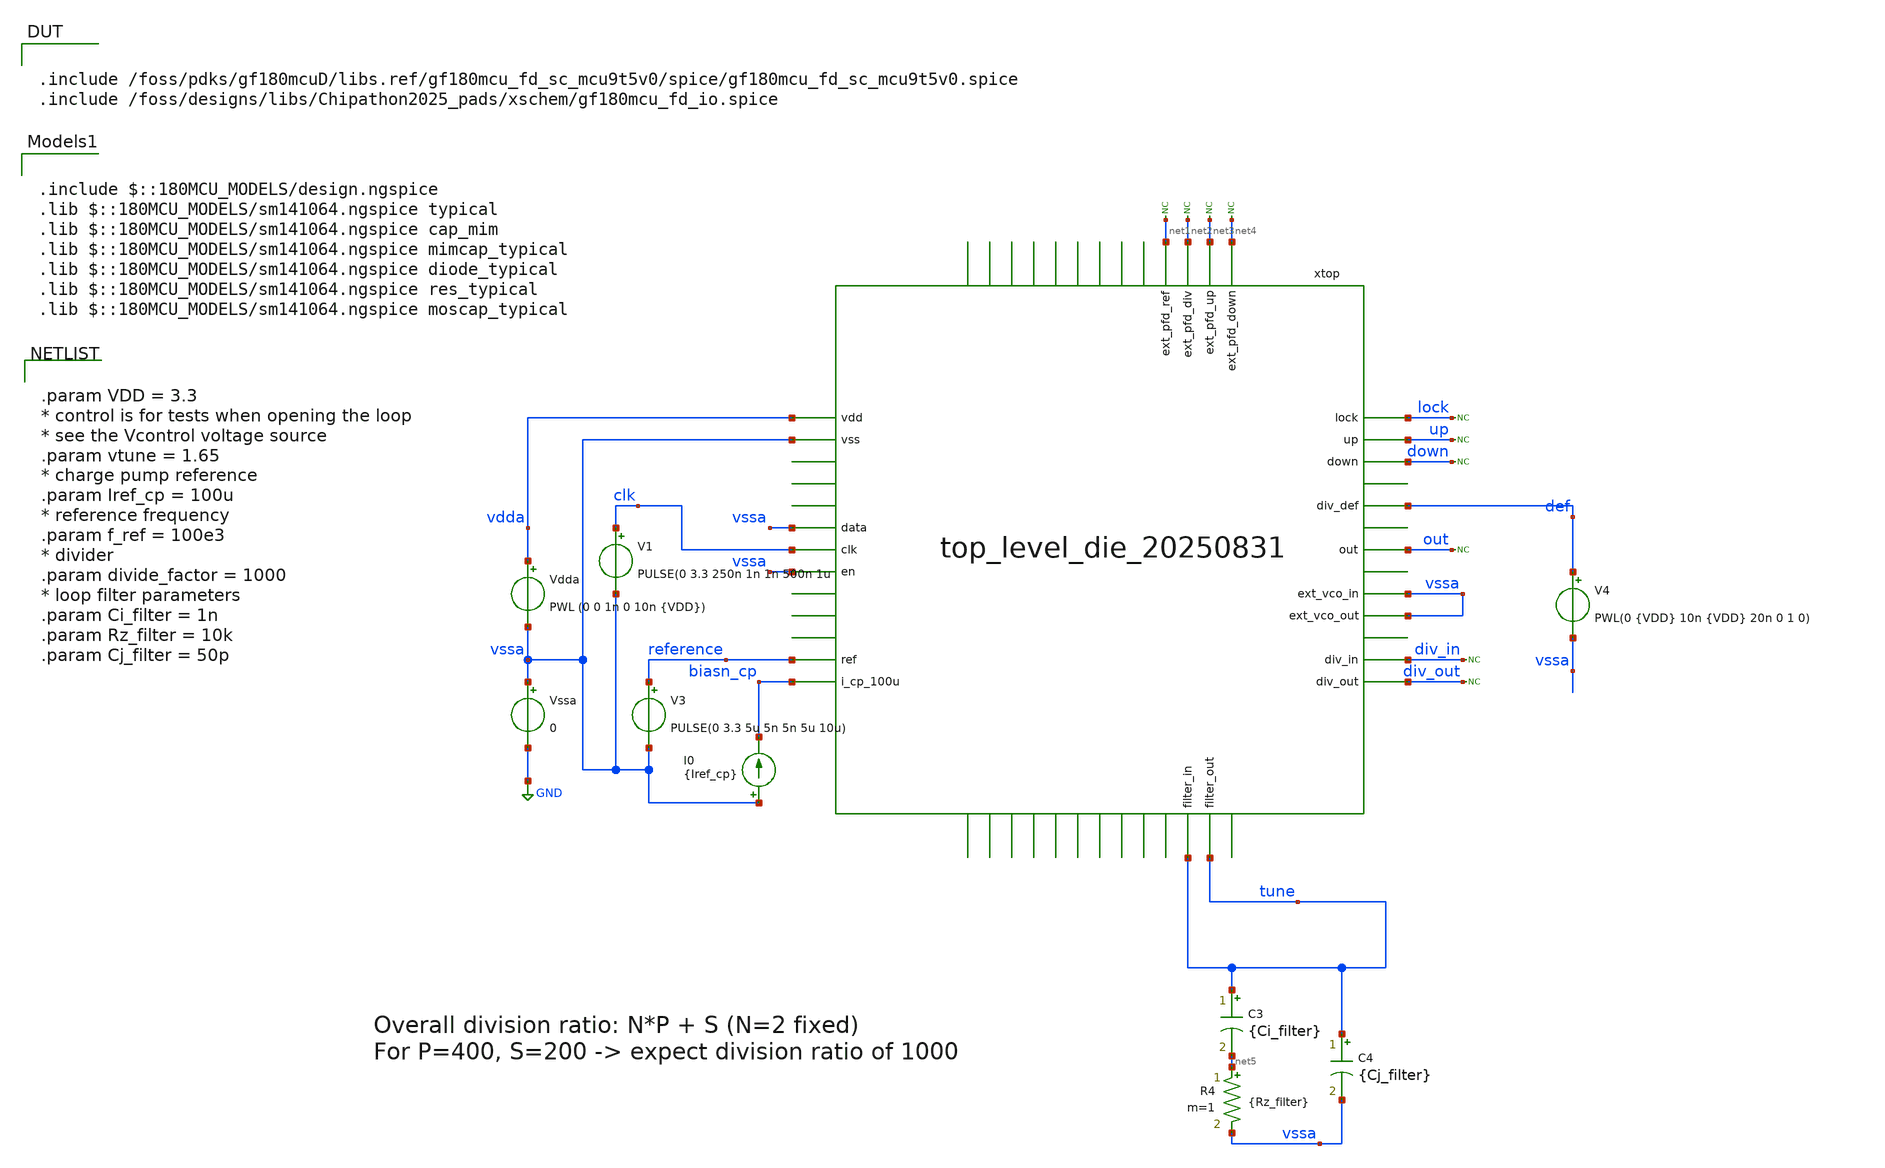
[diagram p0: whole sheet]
** sch_path: designs/libs/tb_top_level/tb_top_level_20250831_die.sch
**.subckt tb_top_level_20250831_die
Vssa vssa GND 0
Vdda vdda vssa PWL (0 0 1n 0 10n {VDD})
I0 vssa biasn_cp {Iref_cp}
V4 def vssa PWL(0 {VDD} 10n {VDD} 20n 0 1 0)
* noconn #net1
* noconn #net2
* noconn #net3
* noconn #net4
* noconn div_in
* noconn div_out
* noconn down
* noconn up
* noconn lock
C3 tune net5 {Ci_filter} m=1
R4 net5 vssa {Rz_filter} m=1
C4 tune vssa {Cj_filter} m=1
* noconn out
V3 reference vssa PULSE(0 3.3 5u 5n 5n 5u 10u)
V1 clk vssa PULSE(0 3.3 250n 1n 1n 500n 1u
xtop vdda vssa vssa clk vssa reference biasn_cp net1 net2 net3 net4 lock up down tune vssa div_in
+ div_out out tune vssa def top_level_die_20250831
**** begin user architecture code


.save v(tune) v(out) v(reference) v(up) v(down) v(xtop.int_div_out) v(xtop.int_div_in) v(xtop.dff_pfd_ref) v(xtop.dff_pfd_up) v(xtop.up_pre) v(xtop.up_post) v(xtop.down_pre) v(xtop.down_post) v(lock)

.control
set filetype=raw
tran 1n 200u
write tb_top_level_20250826.raw
.endc




.param VDD = 3.3
* control is for tests when opening the loop
* see the Vcontrol voltage source
.param vtune = 1.65
* charge pump reference
.param Iref_cp = 100u
* reference frequency
.param f_ref = 100e3
* divider
.param divide_factor = 1000
* loop filter parameters
.param Ci_filter = 1n
.param Rz_filter = 10k
.param Cj_filter = 50p



.include $::180MCU_MODELS/design.ngspice
.lib $::180MCU_MODELS/sm141064.ngspice typical
.lib $::180MCU_MODELS/sm141064.ngspice cap_mim
.lib $::180MCU_MODELS/sm141064.ngspice mimcap_typical
.lib $::180MCU_MODELS/sm141064.ngspice diode_typical
.lib $::180MCU_MODELS/sm141064.ngspice res_typical
.lib $::180MCU_MODELS/sm141064.ngspice moscap_typical


.include /foss/pdks/gf180mcuD/libs.ref/gf180mcu_fd_sc_mcu9t5v0/spice/gf180mcu_fd_sc_mcu9t5v0.spice
.include /foss/designs/libs/Chipathon2025_pads/xschem/gf180mcu_fd_io.spice

**** end user architecture code
**.ends
.GLOBAL GND
.end
